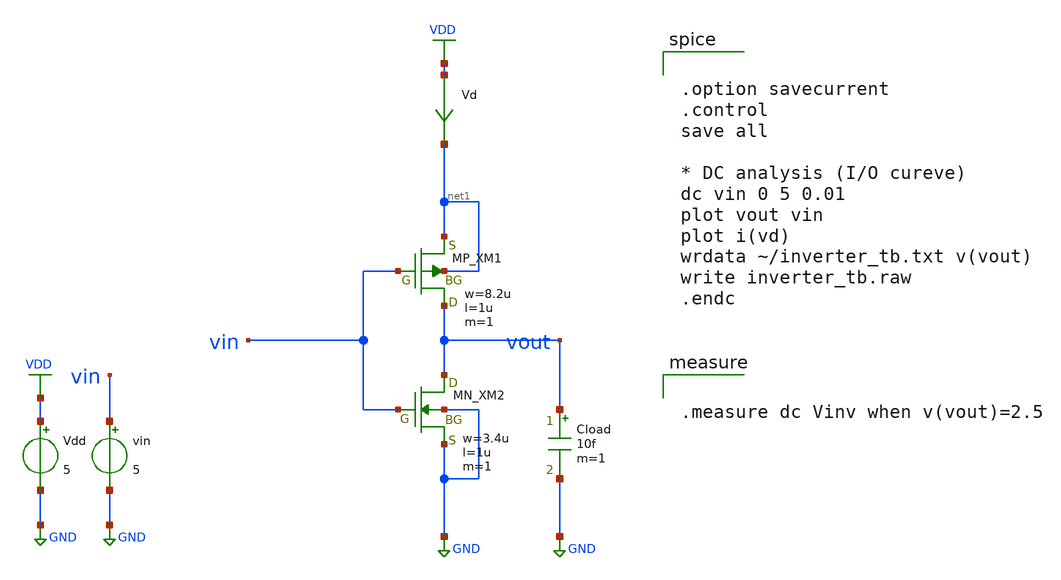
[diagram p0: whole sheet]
** sch_path: inverter/inverter_Satoshi_Kawakami_tb.sch
**.subckt inverter_Satoshi_Kawakami_tb
XXM1 vout vin net1 net1 PMOS w=8.2u l=1u nrd=0 nrs=0 m=1
XXM2 vout vin GND GND NMOS w=3.4u l=1u nrd=0 nrs=0 m=1
Vd VDD net1 0
.save i(vd)
Vdd VDD GND 5
vin vin GND 5
Cload vout GND 10f m=1
**** begin user architecture code
 .include $::LIB/ip62_models


.option savecurrent
.control
save all

* DC analysis (I/O cureve)
dc vin 0 5 0.01
plot vout vin
plot i(vd)
wrdata ~/inverter_tb.txt v(vout)
write inverter_tb.raw
.endc




.measure dc Vinv when v(vout)=2.5


**** end user architecture code
**.ends
.GLOBAL VDD
.GLOBAL GND
.end
